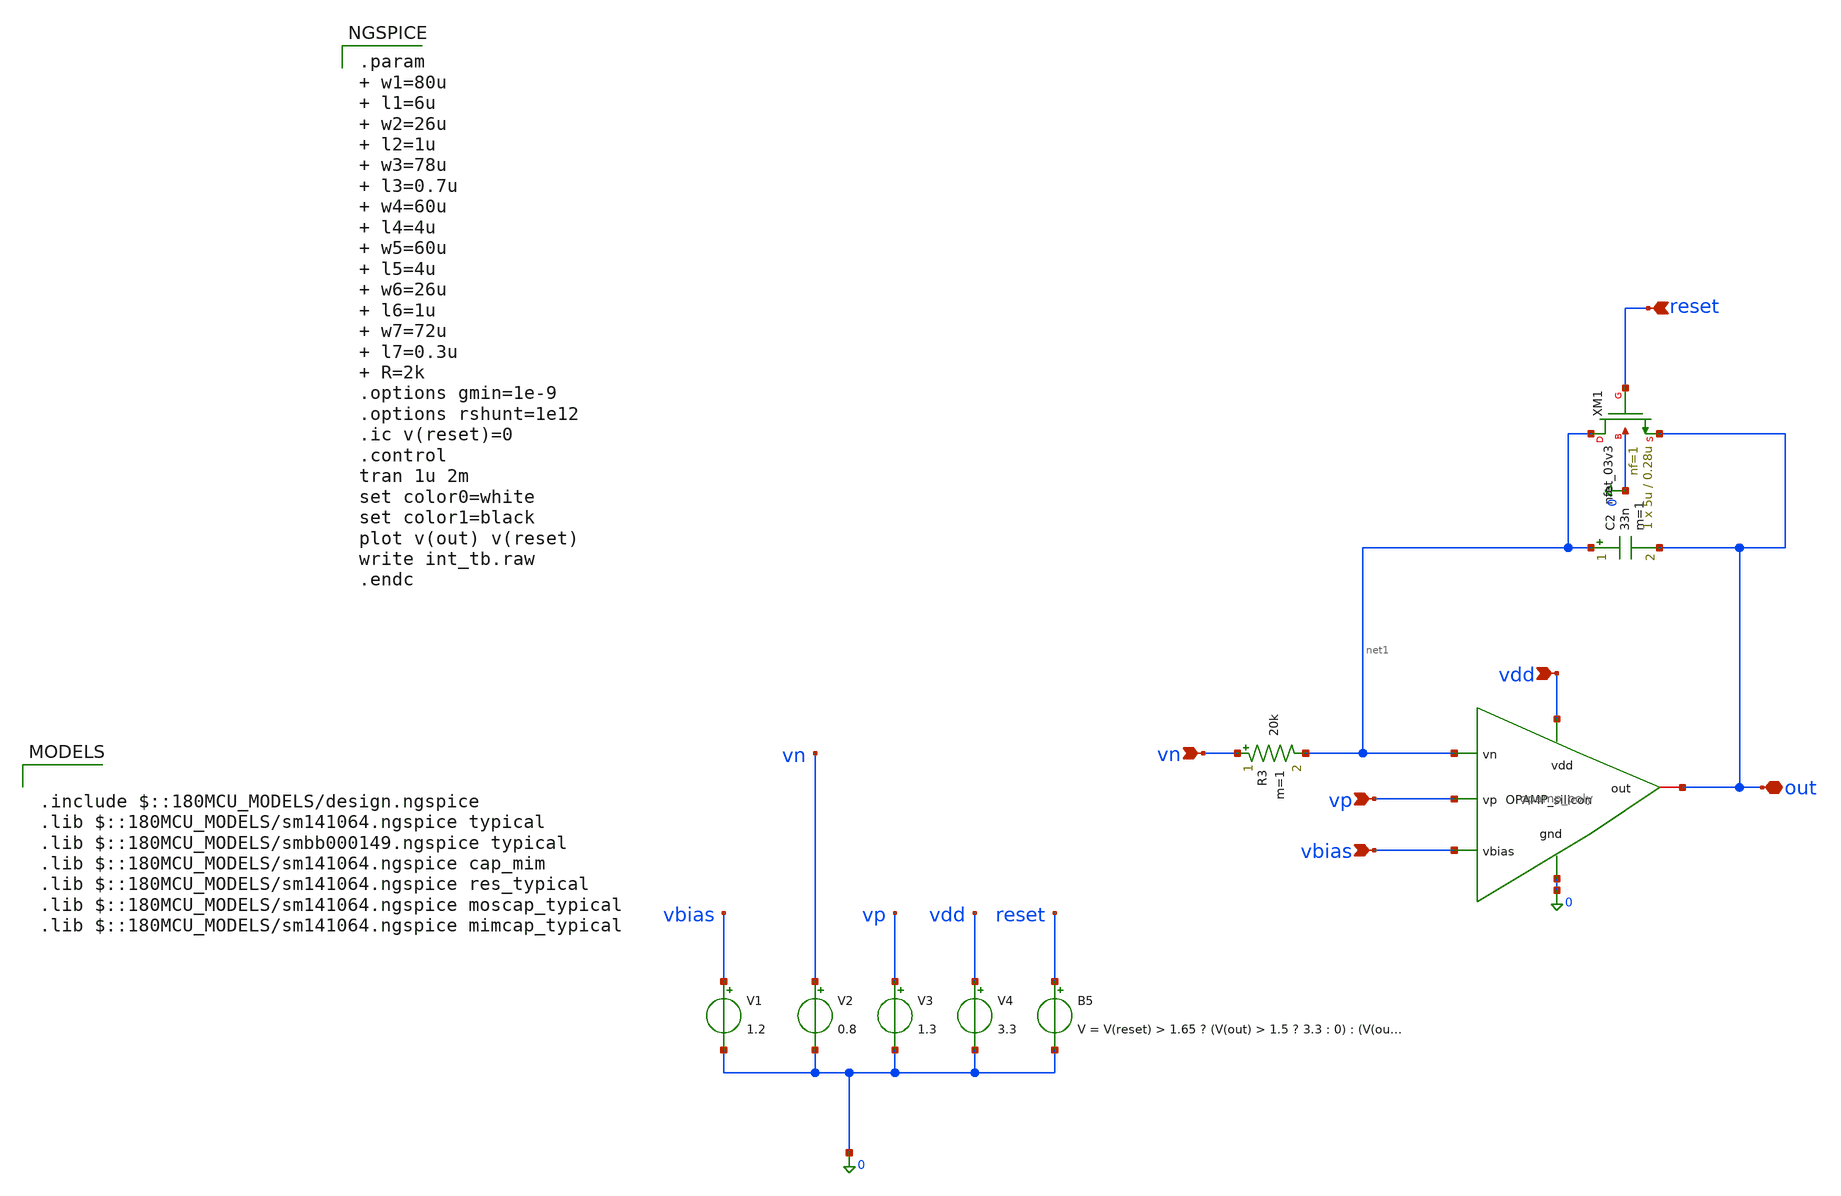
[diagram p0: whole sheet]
** sch_path: xschem/mox_integrator/int_tb.sch
**.subckt int_tb vbias vp vn vdd out reset
*.ipin vbias
*.ipin vp
*.ipin vn
*.ipin vdd
*.iopin out
*.ipin reset
V1 vbias 0 1.2
V3 vp 0 1.3
V4 vdd 0 3.3
C2 net1 out 33n m=1
XM1 net1 reset out 0 nfet_03v3 L=0.28u W=5u nf=1 ad='int((nf+1)/2) * W/nf * 0.18u' as='int((nf+2)/2) * W/nf * 0.18u'
+ pd='2*int((nf+1)/2) * (W/nf + 0.18u)' ps='2*int((nf+2)/2) * (W/nf + 0.18u)' nrd='0.18u / W' nrs='0.18u / W'
+ sa=0 sb=0 sd=0 m=1
x1 vdd net1 0 out vp vbias opamp_poly
R3 vn net1 20k m=1
V2 vn 0 0.8
B5 reset 0 V = V(reset) > 1.65 ? (V(out) > 1.5 ? 3.3 : 0) : (V(out) > 2.5 ? 3.3 : 0)
**** begin user architecture code

.param  w1=80u       l1=6u  w2=26u       l2=1u  w3=78u     l3=0.7u  w4=60u       l4=4u  w5=60u
+      l5=4u  w6=26u       l6=1u  w7=72u    l7=0.3u  R=2k
.options gmin=1e-9
.options rshunt=1e12
.ic v(reset)=0
.control
tran 1u 2m
set color0=white
set color1=black
plot v(out) v(reset)
write int_tb.raw
.endc




.include $::180MCU_MODELS/design.ngspice
.lib $::180MCU_MODELS/sm141064.ngspice typical
.lib $::180MCU_MODELS/smbb000149.ngspice typical
.lib $::180MCU_MODELS/sm141064.ngspice cap_mim
.lib $::180MCU_MODELS/sm141064.ngspice res_typical
.lib $::180MCU_MODELS/sm141064.ngspice moscap_typical
.lib $::180MCU_MODELS/sm141064.ngspice mimcap_typical

**** end user architecture code
**.ends

* expanding   symbol:  GF180/xschem/Chipathon/OpAMP_Silicon/opamp_poly.sym # of pins=6
** sym_path: OpAmP/opamp_poly.sym
** sch_path: OpAmP/opamp_poly.sch
.subckt opamp_poly vdd vn gnd out vp vbias
*.ipin gnd
*.iopin out
*.ipin vbias
*.ipin vp
*.ipin vn
*.ipin vdd
XM1 net3 vbias gnd gnd nfet_03v3 L=l1 W=w1 nf=1 ad='int((nf+1)/2) * W/nf * 0.18u' as='int((nf+2)/2) * W/nf * 0.18u'
+ pd='2*int((nf+1)/2) * (W/nf + 0.18u)' ps='2*int((nf+2)/2) * (W/nf + 0.18u)' nrd='0.18u / W' nrs='0.18u / W'
+ sa=0 sb=0 sd=0 m=1
XM2 net2 net2 vdd vdd pfet_03v3 L=l2 W=w2 nf=1 ad='int((nf+1)/2) * W/nf * 0.18u' as='int((nf+2)/2) * W/nf * 0.18u'
+ pd='2*int((nf+1)/2) * (W/nf + 0.18u)' ps='2*int((nf+2)/2) * (W/nf + 0.18u)' nrd='0.18u / W' nrs='0.18u / W'
+ sa=0 sb=0 sd=0 m=1
XM3 out vbias gnd gnd nfet_03v3 L=l3 W=w3 nf=1 ad='int((nf+1)/2) * W/nf * 0.18u' as='int((nf+2)/2) * W/nf * 0.18u'
+ pd='2*int((nf+1)/2) * (W/nf + 0.18u)' ps='2*int((nf+2)/2) * (W/nf + 0.18u)' nrd='0.18u / W' nrs='0.18u / W'
+ sa=0 sb=0 sd=0 m=1
XM4 net2 vn net3 gnd nfet_03v3 L=l4 W=w4 nf=1 ad='int((nf+1)/2) * W/nf * 0.18u' as='int((nf+2)/2) * W/nf * 0.18u'
+ pd='2*int((nf+1)/2) * (W/nf + 0.18u)' ps='2*int((nf+2)/2) * (W/nf + 0.18u)' nrd='0.18u / W' nrs='0.18u / W'
+ sa=0 sb=0 sd=0 m=1
XM5 net1 vp net3 gnd nfet_03v3 L=l5 W=w5 nf=1 ad='int((nf+1)/2) * W/nf * 0.18u' as='int((nf+2)/2) * W/nf * 0.18u'
+ pd='2*int((nf+1)/2) * (W/nf + 0.18u)' ps='2*int((nf+2)/2) * (W/nf + 0.18u)' nrd='0.18u / W' nrs='0.18u / W'
+ sa=0 sb=0 sd=0 m=1
XM6 net1 net2 vdd vdd pfet_03v3 L=l6 W=w6 nf=1 ad='int((nf+1)/2) * W/nf * 0.18u' as='int((nf+2)/2) * W/nf * 0.18u'
+ pd='2*int((nf+1)/2) * (W/nf + 0.18u)' ps='2*int((nf+2)/2) * (W/nf + 0.18u)' nrd='0.18u / W' nrs='0.18u / W'
+ sa=0 sb=0 sd=0 m=1
XM7 out net1 vdd vdd pfet_03v3 L=l7 W=w7 nf=1 ad='int((nf+1)/2) * W/nf * 0.18u' as='int((nf+2)/2) * W/nf * 0.18u'
+ pd='2*int((nf+1)/2) * (W/nf + 0.18u)' ps='2*int((nf+2)/2) * (W/nf + 0.18u)' nrd='0.18u / W' nrs='0.18u / W'
+ sa=0 sb=0 sd=0 m=1
XR1 net4 net1 gnd ppolyf_u_1k r_width=3e-6 r_length=6.6e-6 m=1
XC1 out net4 cap_mim_1f5fF c_width=20e-6 c_length=20e-6 m=1
.ends

.end
